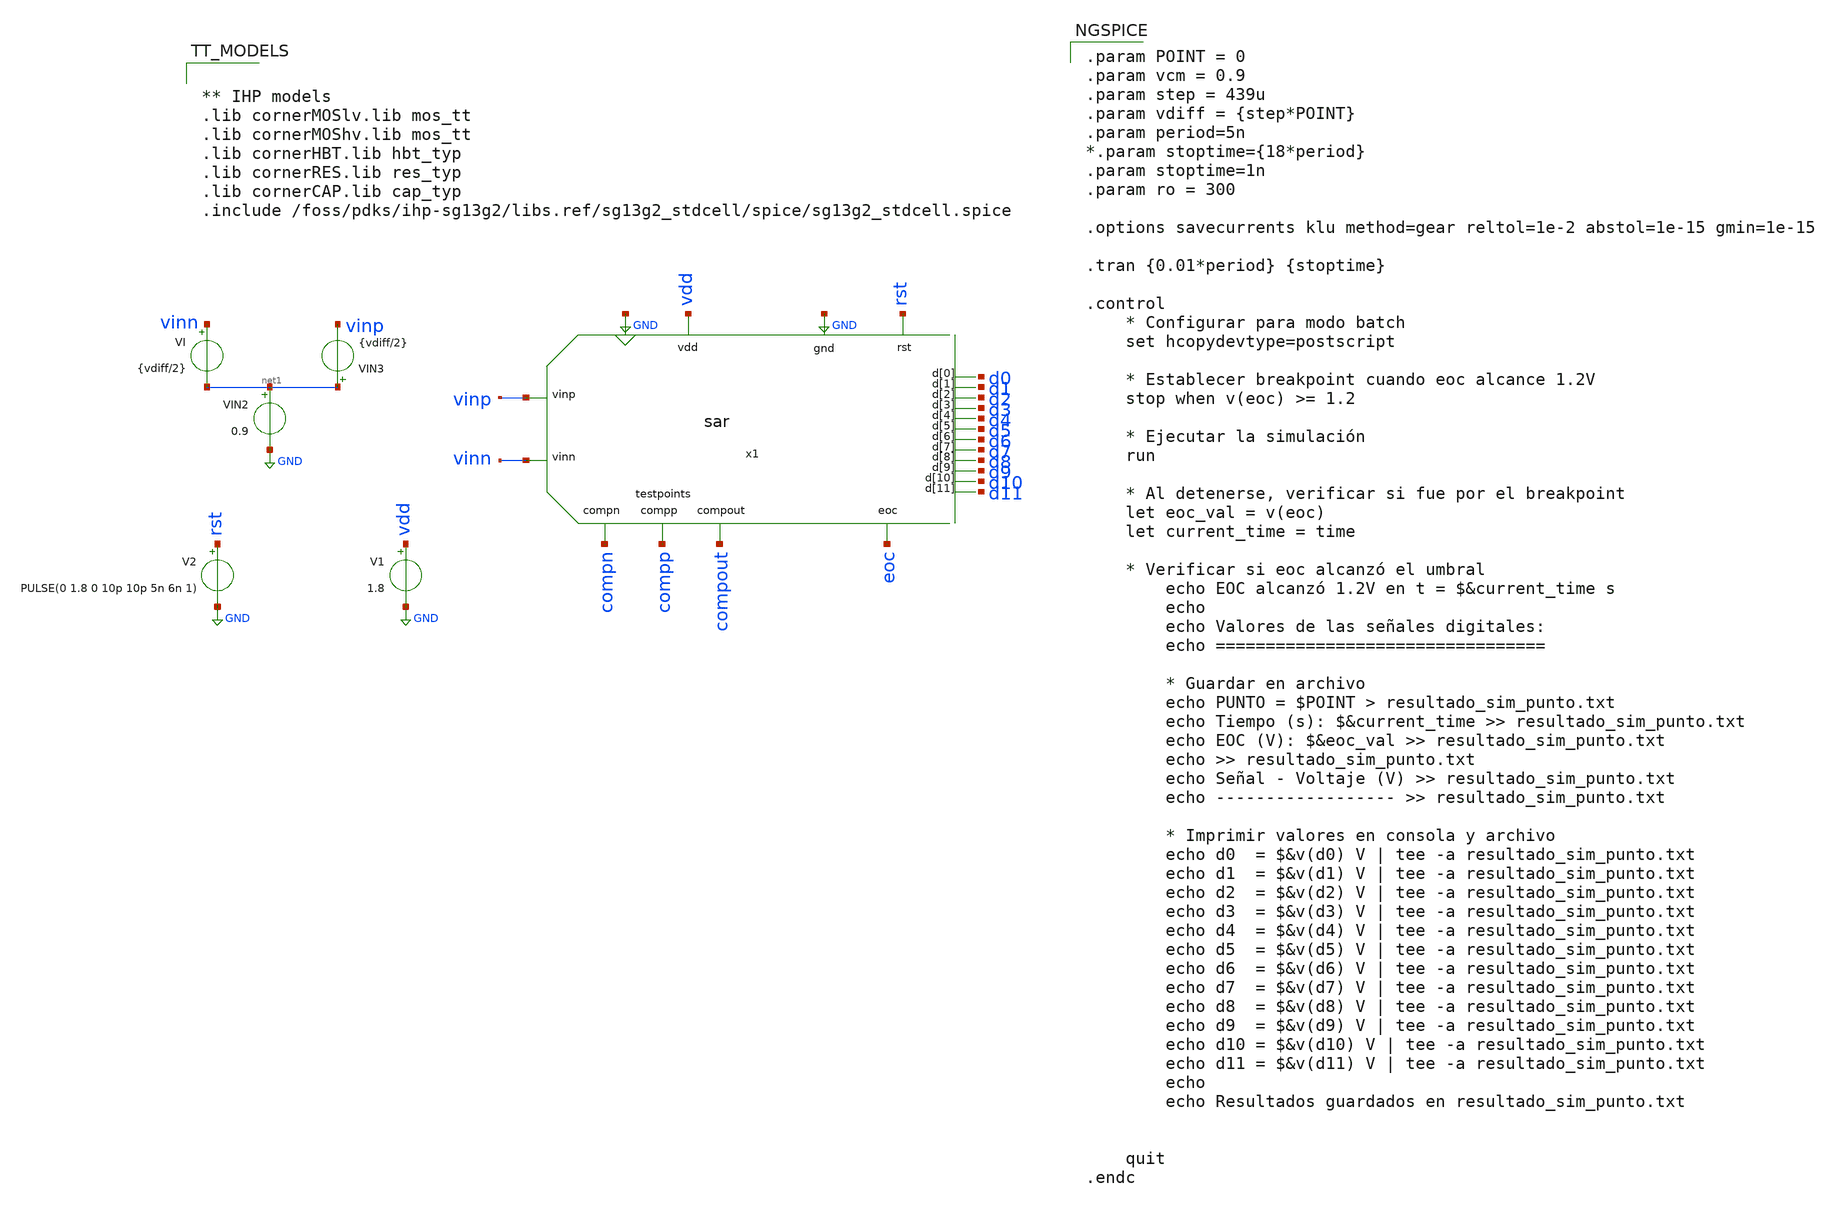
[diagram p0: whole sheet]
** sch_path: xschem/SAR_ADC/testbench/tb_sar_adc_param.sch
**.subckt tb_sar_adc_param
x1 vinp rst GND vinn GND vdd compn compp compout eoc d9 d7 d0 d11 d3 d4 d2 d1 d8 d6 d5 d10 sar
VI vinn net1 {vdiff/2}
V1 vdd GND 1.8
VIN2 net1 GND 0.9
VIN3 net1 vinp {vdiff/2}
V2 rst GND PULSE(0 1.8 0 10p 10p 5n 6n 1)
**** begin user architecture code

.param POINT = 0
.param vcm = 0.9
.param step = 439u
.param vdiff = {step*POINT}
.param period=5n
*.param stoptime={18*period}
.param stoptime=1n
.param ro = 300

.options savecurrents klu method=gear reltol=1e-2 abstol=1e-15 gmin=1e-15

.tran {0.01*period} {stoptime}

.control
    * Configurar para modo batch
    set hcopydevtype=postscript

    * Establecer breakpoint cuando eoc alcance 1.2V
    stop when v(eoc) >= 1.2

    * Ejecutar la simulación
    run

    * Al detenerse, verificar si fue por el breakpoint
    let eoc_val = v(eoc)
    let current_time = time

    * Verificar si eoc alcanzó el umbral
        echo EOC alcanzó 1.2V en t = $&current_time s
        echo
        echo Valores de las señales digitales:
        echo =================================

        * Guardar en archivo
        echo PUNTO = $POINT > resultado_sim_punto.txt
        echo Tiempo (s): $&current_time >> resultado_sim_punto.txt
        echo EOC (V): $&eoc_val >> resultado_sim_punto.txt
        echo >> resultado_sim_punto.txt
        echo Señal - Voltaje (V) >> resultado_sim_punto.txt
        echo ------------------ >> resultado_sim_punto.txt

        * Imprimir valores en consola y archivo
        echo d0  = $&v(d0) V | tee -a resultado_sim_punto.txt
        echo d1  = $&v(d1) V | tee -a resultado_sim_punto.txt
        echo d2  = $&v(d2) V | tee -a resultado_sim_punto.txt
        echo d3  = $&v(d3) V | tee -a resultado_sim_punto.txt
        echo d4  = $&v(d4) V | tee -a resultado_sim_punto.txt
        echo d5  = $&v(d5) V | tee -a resultado_sim_punto.txt
        echo d6  = $&v(d6) V | tee -a resultado_sim_punto.txt
        echo d7  = $&v(d7) V | tee -a resultado_sim_punto.txt
        echo d8  = $&v(d8) V | tee -a resultado_sim_punto.txt
        echo d9  = $&v(d9) V | tee -a resultado_sim_punto.txt
        echo d10 = $&v(d10) V | tee -a resultado_sim_punto.txt
        echo d11 = $&v(d11) V | tee -a resultado_sim_punto.txt
        echo
        echo Resultados guardados en resultado_sim_punto.txt


    quit
.endc




** IHP models
.lib cornerMOSlv.lib mos_tt
.lib cornerMOShv.lib mos_tt
.lib cornerHBT.lib hbt_typ
.lib cornerRES.lib res_typ
.lib cornerCAP.lib cap_typ
.include /foss/pdks/ihp-sg13g2/libs.ref/sg13g2_stdcell/spice/sg13g2_stdcell.spice


**** end user architecture code
**.ends
.GLOBAL GND
.end
